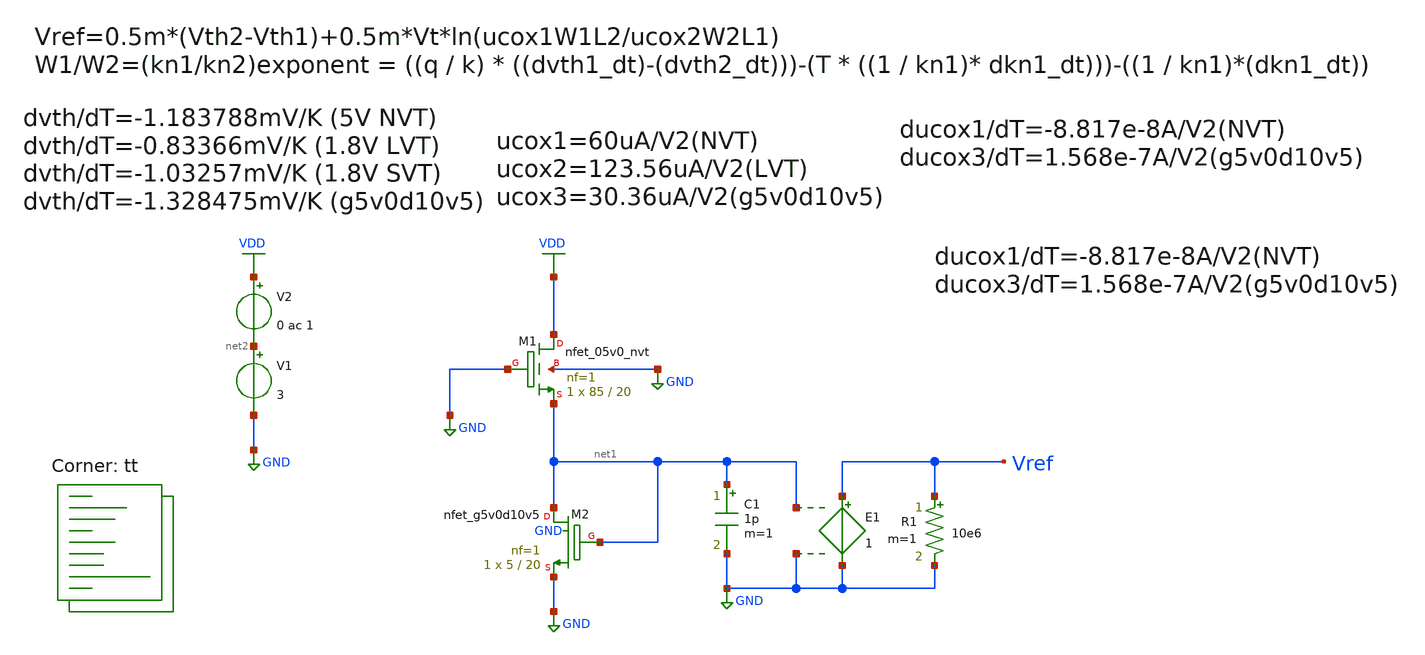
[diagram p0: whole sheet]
** sch_path: 2TBGR/Schematics/2tbgr1try.sch
**.subckt 2tbgr1try
XM1 VDD GND net1 GND sky130_fd_pr__nfet_05v0_nvt L=20 W=85 nf=1 ad='int((nf+1)/2) * W/nf * 0.29' as='int((nf+2)/2) * W/nf * 0.29'
+ pd='2*int((nf+1)/2) * (W/nf + 0.29)' ps='2*int((nf+2)/2) * (W/nf + 0.29)' nrd='0.29 / W' nrs='0.29 / W'
+ sa=0 sb=0 sd=0 mult=1 m=1
XM2 net1 net1 GND GND sky130_fd_pr__nfet_g5v0d10v5 L=20 W=5 nf=1 ad='int((nf+1)/2) * W/nf * 0.29' as='int((nf+2)/2) * W/nf * 0.29'
+ pd='2*int((nf+1)/2) * (W/nf + 0.29)' ps='2*int((nf+2)/2) * (W/nf + 0.29)' nrd='0.29 / W' nrs='0.29 / W'
+ sa=0 sb=0 sd=0 mult=1 m=1
V1 net2 GND 3
V2 VDD net2 0 ac 1
C1 net1 GND 1p m=1
R1 Vref GND 10e6 m=1
E1 Vref GND net1 GND 1
**** begin user architecture code
.lib $::SKYWATER_MODELS/sky130.lib.spice tt


.option wnflag=1
.option savecurrents
.temp 27
.control
save @m.xm1.msky130_fd_pr__nfet_05v0_nvt[gm]
save @m.xm1.msky130_fd_pr__nfet_05v0_nvt[id]
save @m.xm2.msky130_fd_pr__nfet_g5v0d10v5[gm]
save @m.xm2.msky130_fd_pr__nfet_g5v0d10v5[id]
save all
write 2tbgr1try.raw
set appendwrite
op
write 2tbgr1try.raw
dc temp -50 150 1
**ac dec 20 1 1e8
plot v(Vref)
.endc

**** end user architecture code
**.ends
.GLOBAL GND
.GLOBAL VDD
.end
